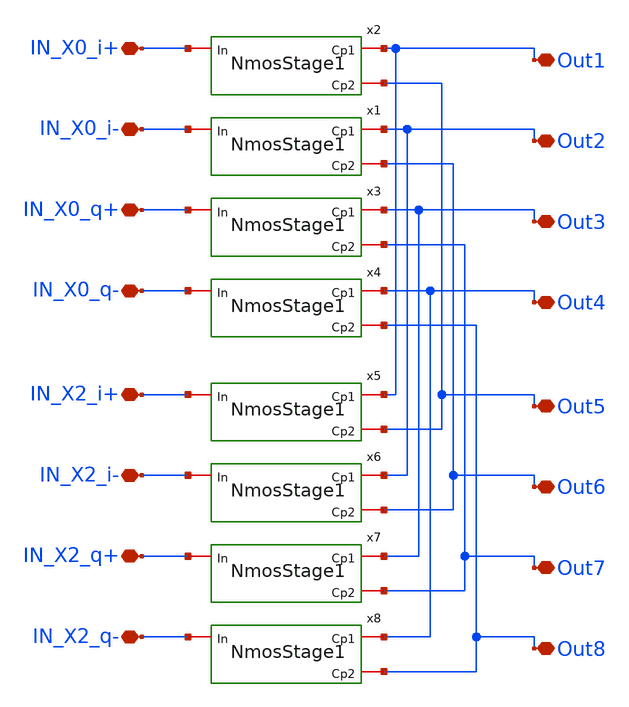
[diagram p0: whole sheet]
** sch_path: xschem/FinalProject/NMOSR2Stg1.sch
**.subckt NMOSR2Stg1 IN_X0_i+ Out1 IN_X0_i- Out2 IN_X0_q+ Out3 IN_X0_q- Out4 IN_X2_i+ Out5 IN_X2_i-
*+ Out6 IN_X2_q+ Out7 IN_X2_q- Out8
*.iopin IN_X0_i+
*.iopin Out1
*.iopin IN_X0_i-
*.iopin Out2
*.iopin IN_X0_q+
*.iopin Out3
*.iopin IN_X0_q-
*.iopin Out4
*.iopin IN_X2_i+
*.iopin Out5
*.iopin IN_X2_i-
*.iopin Out6
*.iopin IN_X2_q+
*.iopin Out7
*.iopin IN_X2_q-
*.iopin Out8
x2 IN_X0_i+ Out1 Out5 NmosStage1
x1 IN_X0_i- Out2 Out6 NmosStage1
x3 IN_X0_q+ Out3 Out7 NmosStage1
x4 IN_X0_q- Out4 Out8 NmosStage1
x5 IN_X2_i+ Out1 Out5 NmosStage1
x6 IN_X2_i- Out2 Out6 NmosStage1
x7 IN_X2_q+ Out3 Out7 NmosStage1
x8 IN_X2_q- Out4 Out8 NmosStage1
**** begin user architecture code

** opencircuitdesign pdks install
.lib $::SKYWATER_MODELS/sky130.lib.spice tt



* this option enables mos model bin
* selection based on W/NF instead of W
.control
op
*dc VDD 1 4 0.01
print all
save all
.endc


**** end user architecture code
**.ends
.end
